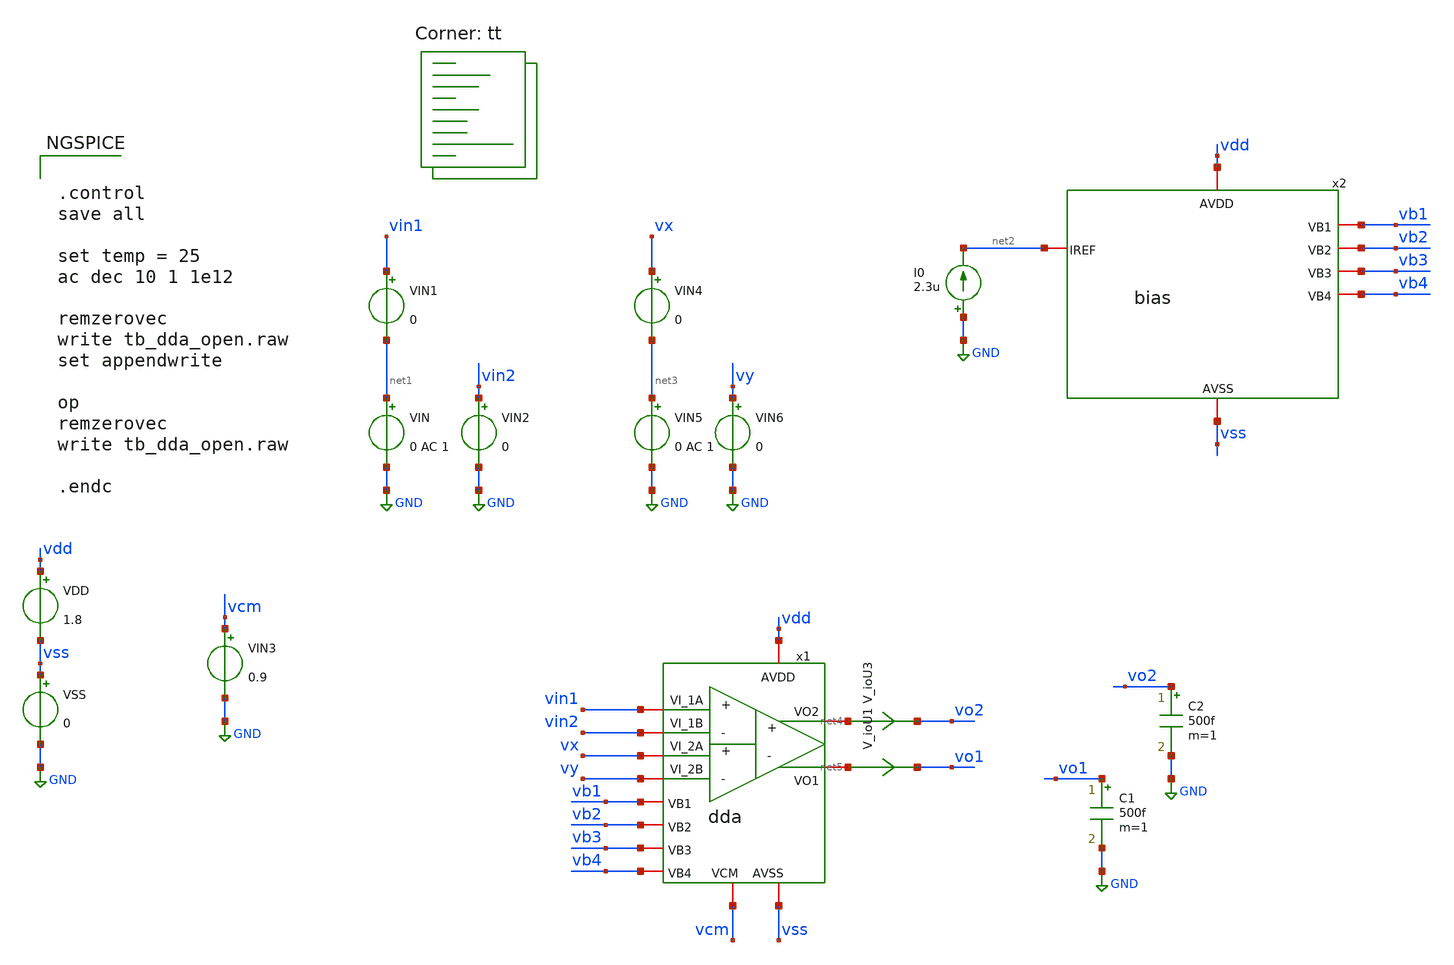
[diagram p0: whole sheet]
** sch_path: xschem/testbenches/tb_dda_open.sch
**.subckt tb_dda_open
VDD vdd vss 1.8
VSS vss GND 0
C1 vo1 GND 500f m=1
I0 GND net2 2.3u
VIN1 vin1 net1 0
VIN2 vin2 GND 0
VIN net1 GND 0 AC 1
C2 vo2 GND 500f m=1
VIN3 vcm GND 0.9
V_ioU3 net4 vo2 0
.save i(v_iou3)
V_ioU1 net5 vo1 0
.save i(v_iou1)
x1 vdd vss vin1 vin2 net4 net5 vcm vb1 vb2 vb3 vb4 vx vy dda
x2 net2 vb1 vdd vss vb2 vb3 vb4 bias
VIN4 vx net3 0
VIN5 net3 GND 0 AC 1
VIN6 vy GND 0
**** begin user architecture code


.control
save all

set temp = 25
ac dec 10 1 1e12

remzerovec
write tb_dda_open.raw
set appendwrite

op
remzerovec
write tb_dda_open.raw

.endc


.lib $::SKYWATER_MODELS/sky130.lib.spice tt
**** end user architecture code
**.ends
.GLOBAL GND
.end
